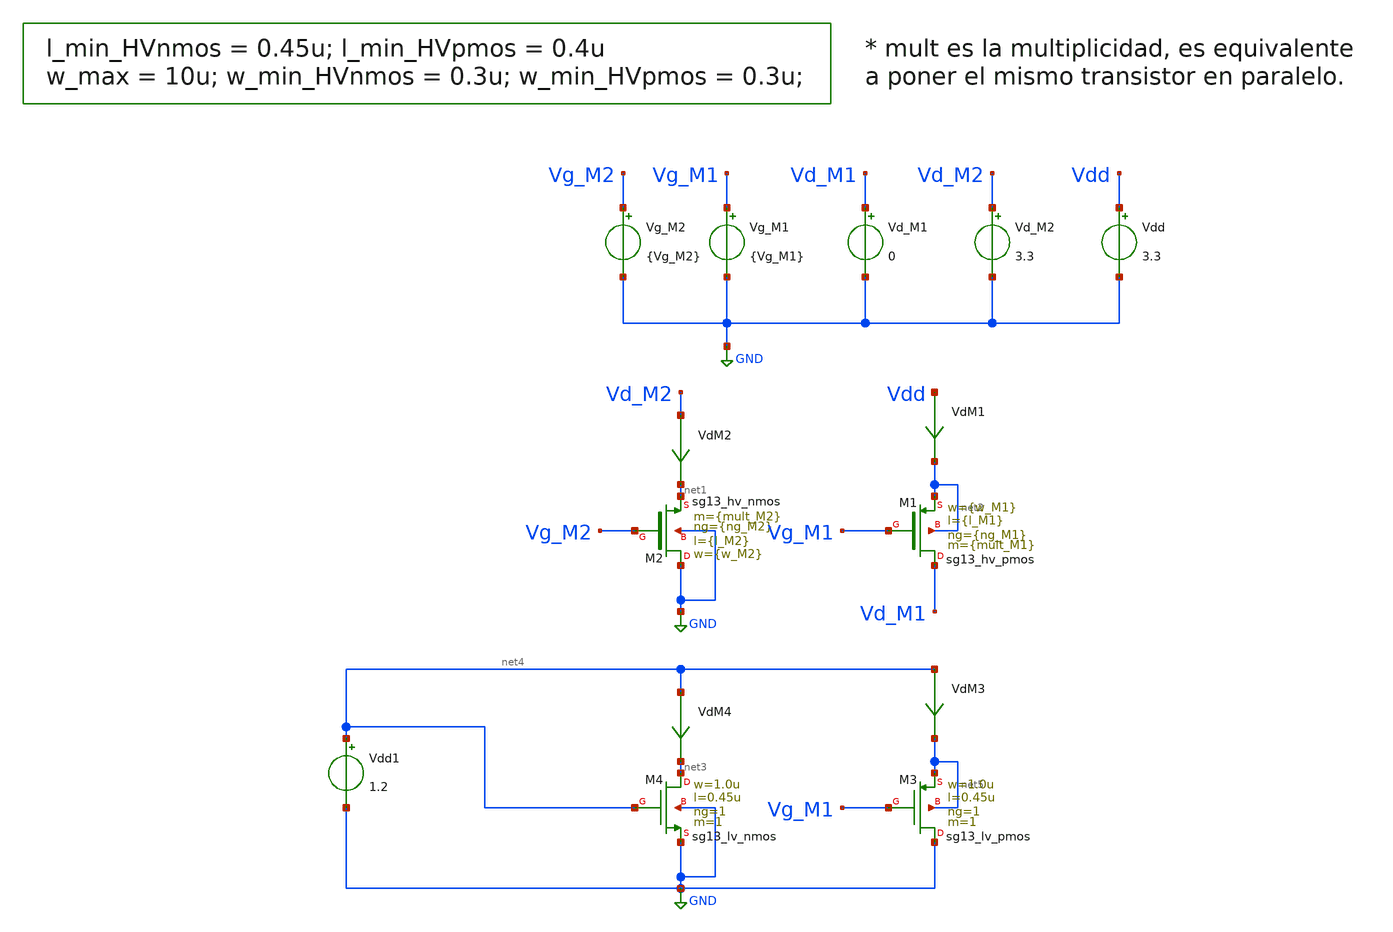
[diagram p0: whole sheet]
** sch_path: xschem/DCDCBuck/TB_hvMOS_POWER_Sizing.sch
**.subckt TB_hvMOS_POWER_Sizing
Vg_M1 Vg_M1 GND {Vg_M1}
Vd_M1 Vd_M1 GND 0
XM2 GND Vg_M2 net1 GND sg13_hv_nmos w={w_M2} l={l_M2} ng={ng_M2} m={mult_M2} mm_ok=1
VdM1 Vdd net2 0
.save i(vdm1)
XM1 Vd_M1 Vg_M1 net2 net2 sg13_hv_pmos w={w_M1} l={l_M1} ng={ng_M1} m={mult_M1} mm_ok=1
VdM2 Vd_M2 net1 0
.save i(vdm2)
Vg_M2 Vg_M2 GND {Vg_M2}
Vd_M2 Vd_M2 GND 3.3
Vdd Vdd GND 3.3
VdM3 net4 net5 0
.save i(vdm3)
VdM4 net4 net3 0
.save i(vdm4)
XM4 net3 net4 GND GND sg13_lv_nmos w=1.0u l=0.45u ng=1 m=1 mm_ok=1
XM3 GND Vg_M1 net5 net5 sg13_lv_pmos w=1.0u l=0.45u ng=1 m=1 mm_ok=1
Vdd1 net4 GND 1.2
**** begin user architecture code


.lib cornerMOShv.lib mos_tt
.lib cornerMOSlv.lib mos_tt
*.lib cornerMOShv.lib mos_ff
*.lib cornerMOSlv.lib mos_ff
*.lib cornerMOShv.lib mos_ss
*.lib cornerMOSlv.lib mos_ss
*.lib cornerMOShv.lib mos_sf
*.lib cornerMOSlv.lib mos_sf
*.lib cornerMOShv.lib mos_fs
*.lib cornerMOSlv.lib mos_fs

*.include /opt/pdks/ihp-sg13g2/libs.ref/sg13g2_stdcell/spice/sg13g2_stdcell.spice
*.lib $::SG13G2_MODELS/cornerRES.lib res_typ
*.lib $::SG13G2_MODELS/cornerCAP.lib cap_typ
*.lib $::SG13G2_MODELS/diodes.lib



.save all

.param Vg_M1 = 0
.param Vg_M2 = 3.3
.csparam V_on = 50m

.control
reset
run
dc Vd_M2 0 1 0.01
*dc Vds 0 0.5 0.01 temp 0 27 1
let Vds_M2 = v(Vd_M2)
let Ids_M2 = i(VdM2)



*let G_M2 = Ids_M2/(Vds_M2+0.01)
let G_M2 = @n.xm2.nsg13_hv_nmos[gds]
let Vth_M2 = @n.xm2.nsg13_hv_nmos[vth]
let Ron_M2 = 1/G_M2
let I_M2 = i(VdM2)
let G_M22 = deriv(I_M2)
let Ron_M22 = 1/G_M22

plot Ron_M2 Ron_M22 vs Vds_M2
plot Ids_M2 vs Vds_M2
*plot Vth_M2 vs Vds_M2

let Vds_on = {V_on}

meas dc Ion_M2 FIND Ids_M2 AT={Vds_on}
meas dc RonM2 FIND Ron_M22 AT={Vds_on}
*write TB_hvMOS_POWER_Sizing_IPD413_202501_HW1.raw IM2 RonM2
.endc


.control
reset
run
dc Vd_M1 2.3 3.3 0.01
*dc Vd_M1 2 1.8 0.01 temp 0 27 1

let Vsd_M1 = v(Vdd) -v(Vd_M1)
let Isd_M1 = i(VdM1)

let G_M1 = @n.xm1.nsg13_hv_pmos[gds]
let G_M11 = deriv(Isd_M1)
let Ron_M11 = -1/G_M11
*let G_M1 = Isd_M1/Vsd_M1
let Ron_M1 = 1/G_M1
let Vth_M1 = @n.xm1.nsg13_hv_pmos[vth]

plot Isd_M1 vs Vsd_M1
plot Ron_M1 Ron_M11 vs Vsd_M1
*plot Vth_M1 vs Vsd_M1

let Vsd_on = 3.3-{V_on}

meas dc Ion_M1 FIND Isd_M1 AT={Vsd_on}
meas dc RonM1 FIND Ron_M11 AT={Vsd_on}


.endc

.control
reset
unset filetype
op
let Vth_M2 = @n.xm2.nsg13_hv_nmos[vth]
let gds_M2 = @n.xm2.nsg13_hv_nmos[gds]
let Vov_M2 = v(Vg_M2) - Vth_M2
let Vth_M1 = @n.xm1.nsg13_hv_pmos[vth]
let gds_M1 = @n.xm1.nsg13_hv_pmos[gds]
let Vov_M1 = v(Vdd)-v(Vg_M1) - Vth_M1
let Vth_M3 = @n.xm3.nsg13_lv_pmos[vth]
let Vth_M4 = @n.xm4.nsg13_lv_nmos[vth]
write TB_hvMOS_POWER_Sizing.raw
.endc

.end




.param mult = 95238
.param temp=27
.param mult_M1 = 3*mult
.param w_M1 =0.3u
.param l_M1 = 0.45u
.param ng_M1 = 1

.param mult_M2 = 1*mult
.param w_M2 =0.3u
.param l_M2 =0.45u
.param ng_M2 =1





**** end user architecture code
**.ends
.GLOBAL GND
.end
